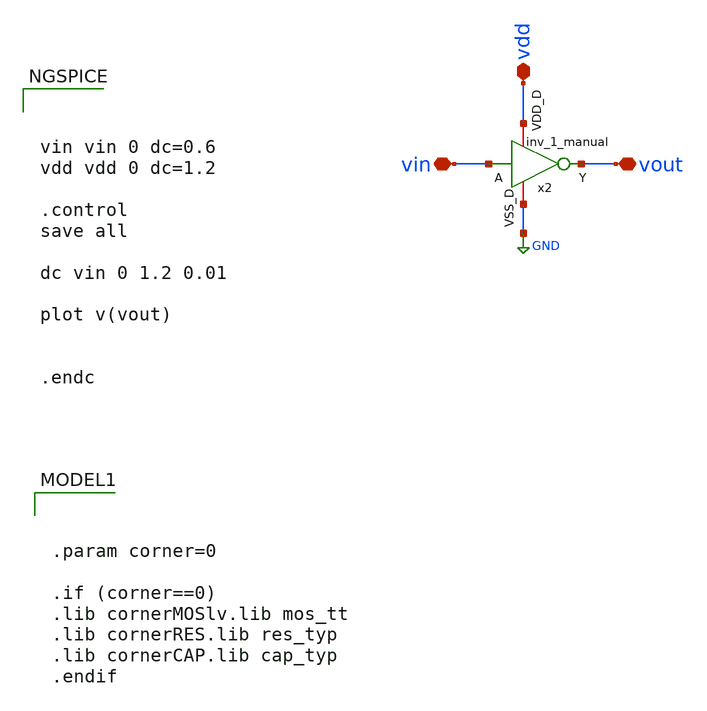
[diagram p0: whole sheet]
** sch_path: DelayLine/others/tb_inv_1_manual.sch
**.subckt tb_inv_1_manual vin vout vdd
*.iopin vin
*.iopin vout
*.iopin vdd
x2 vdd vin vout GND inv_1_manual
**** begin user architecture code



vin vin 0 dc=0.6
vdd vdd 0 dc=1.2

.control
save all

dc vin 0 1.2 0.01

plot v(vout)


.endc




.param corner=0

.if (corner==0)
.lib cornerMOSlv.lib mos_tt
.lib cornerRES.lib res_typ
.lib cornerCAP.lib cap_typ
.endif

**** end user architecture code
**.ends
.GLOBAL GND
.end
